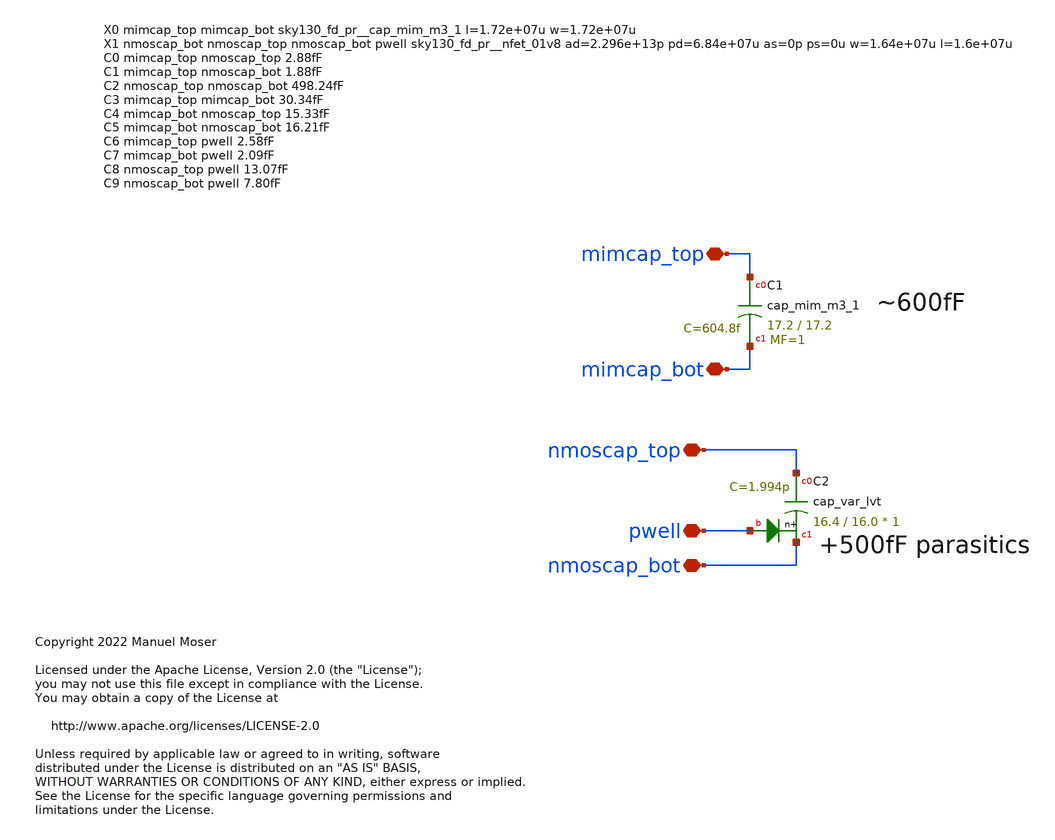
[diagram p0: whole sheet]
** sch_path: xschem/adc_noise_decoup_cell1.sch
* Copyright 2022 Manuel Moser
* Licensed under the Apache License, Version 2.0 (the "License");
**.subckt adc_noise_decoup_cell1 nmoscap_top mimcap_top mimcap_bot nmoscap_bot pwell
*.iopin nmoscap_top
*.iopin mimcap_top
*.iopin mimcap_bot
*.iopin nmoscap_bot
*.iopin pwell
XC1 mimcap_top mimcap_bot sky130_fd_pr__cap_mim_m3_1 W=17.2 L=17.2 MF=1 m=1
XC2 nmoscap_top nmoscap_bot pwell sky130_fd_pr__cap_var_lvt W=16.4 L=16.0 VM=1 m=1
**.ends
.end
